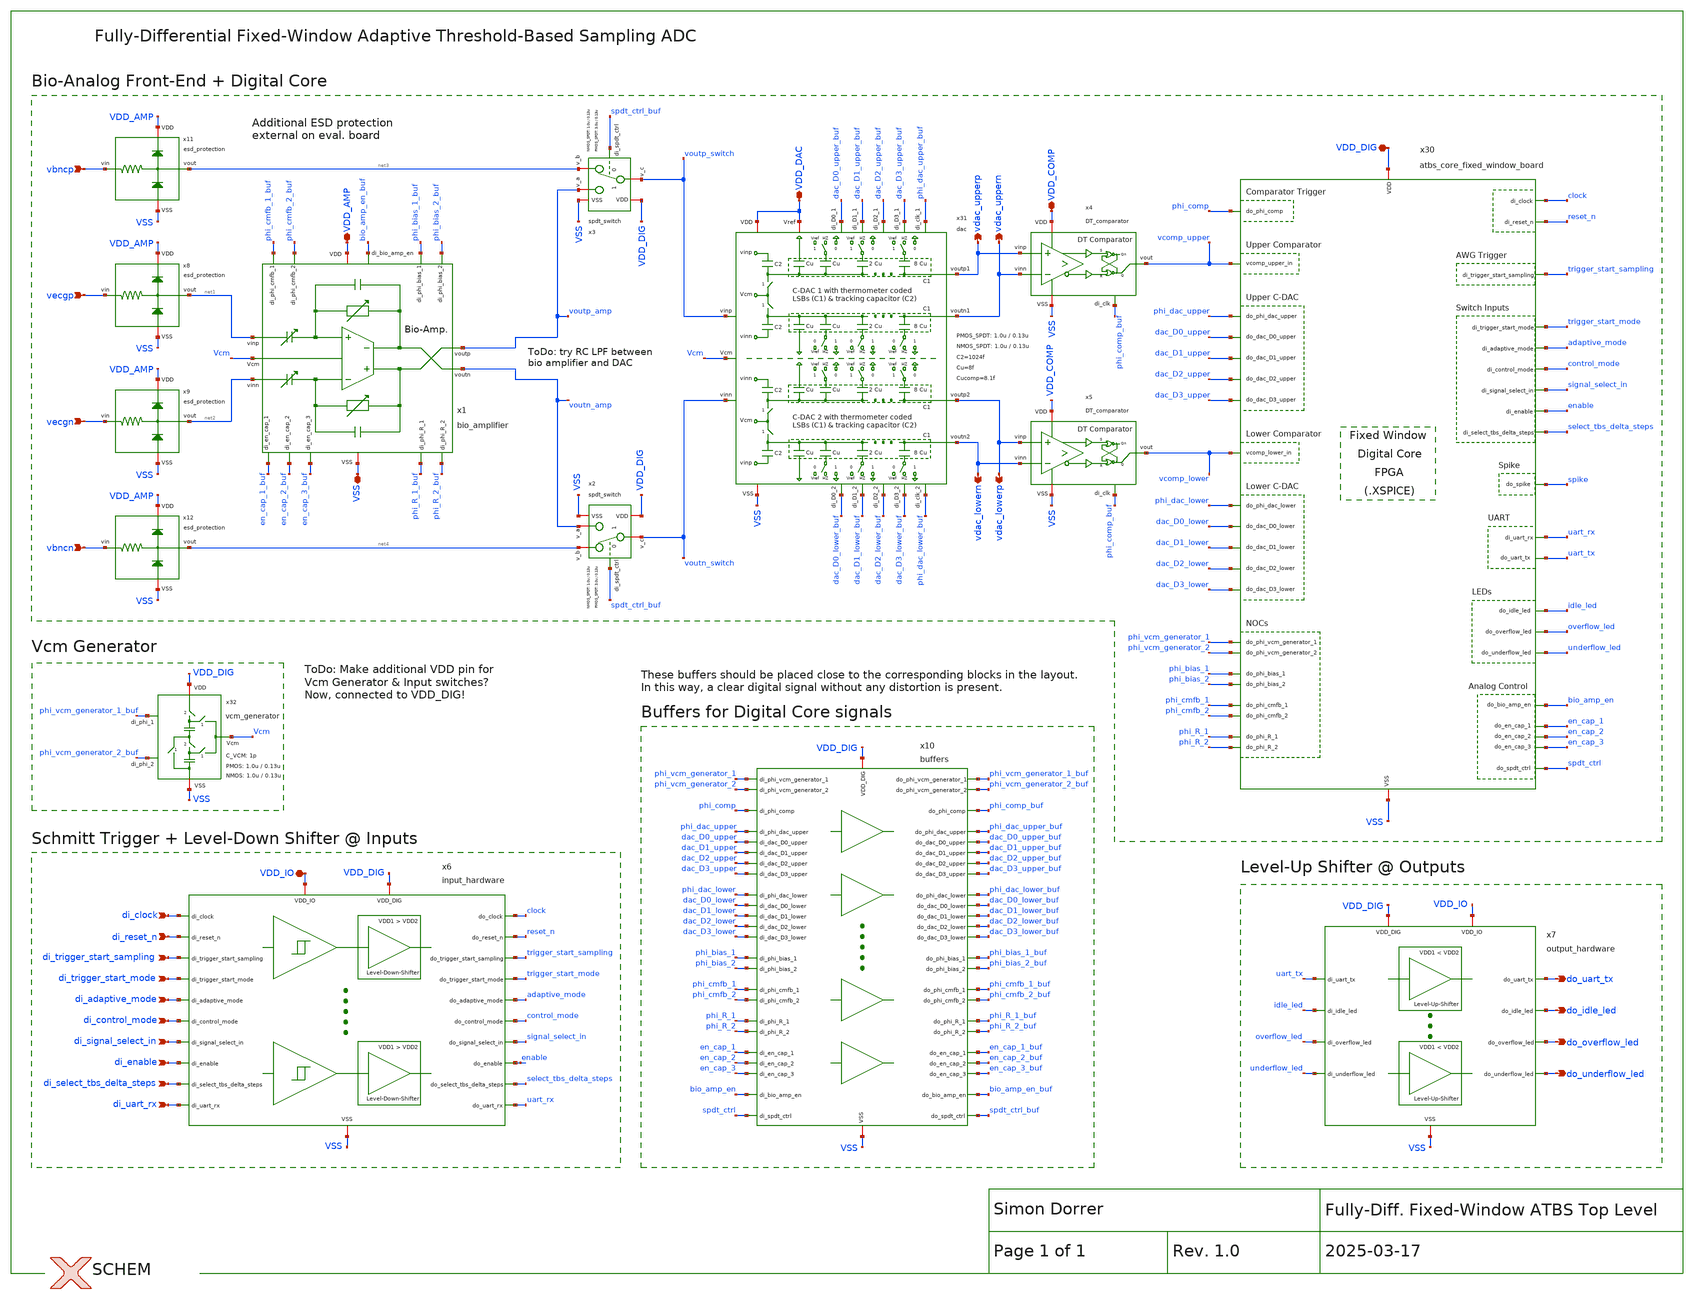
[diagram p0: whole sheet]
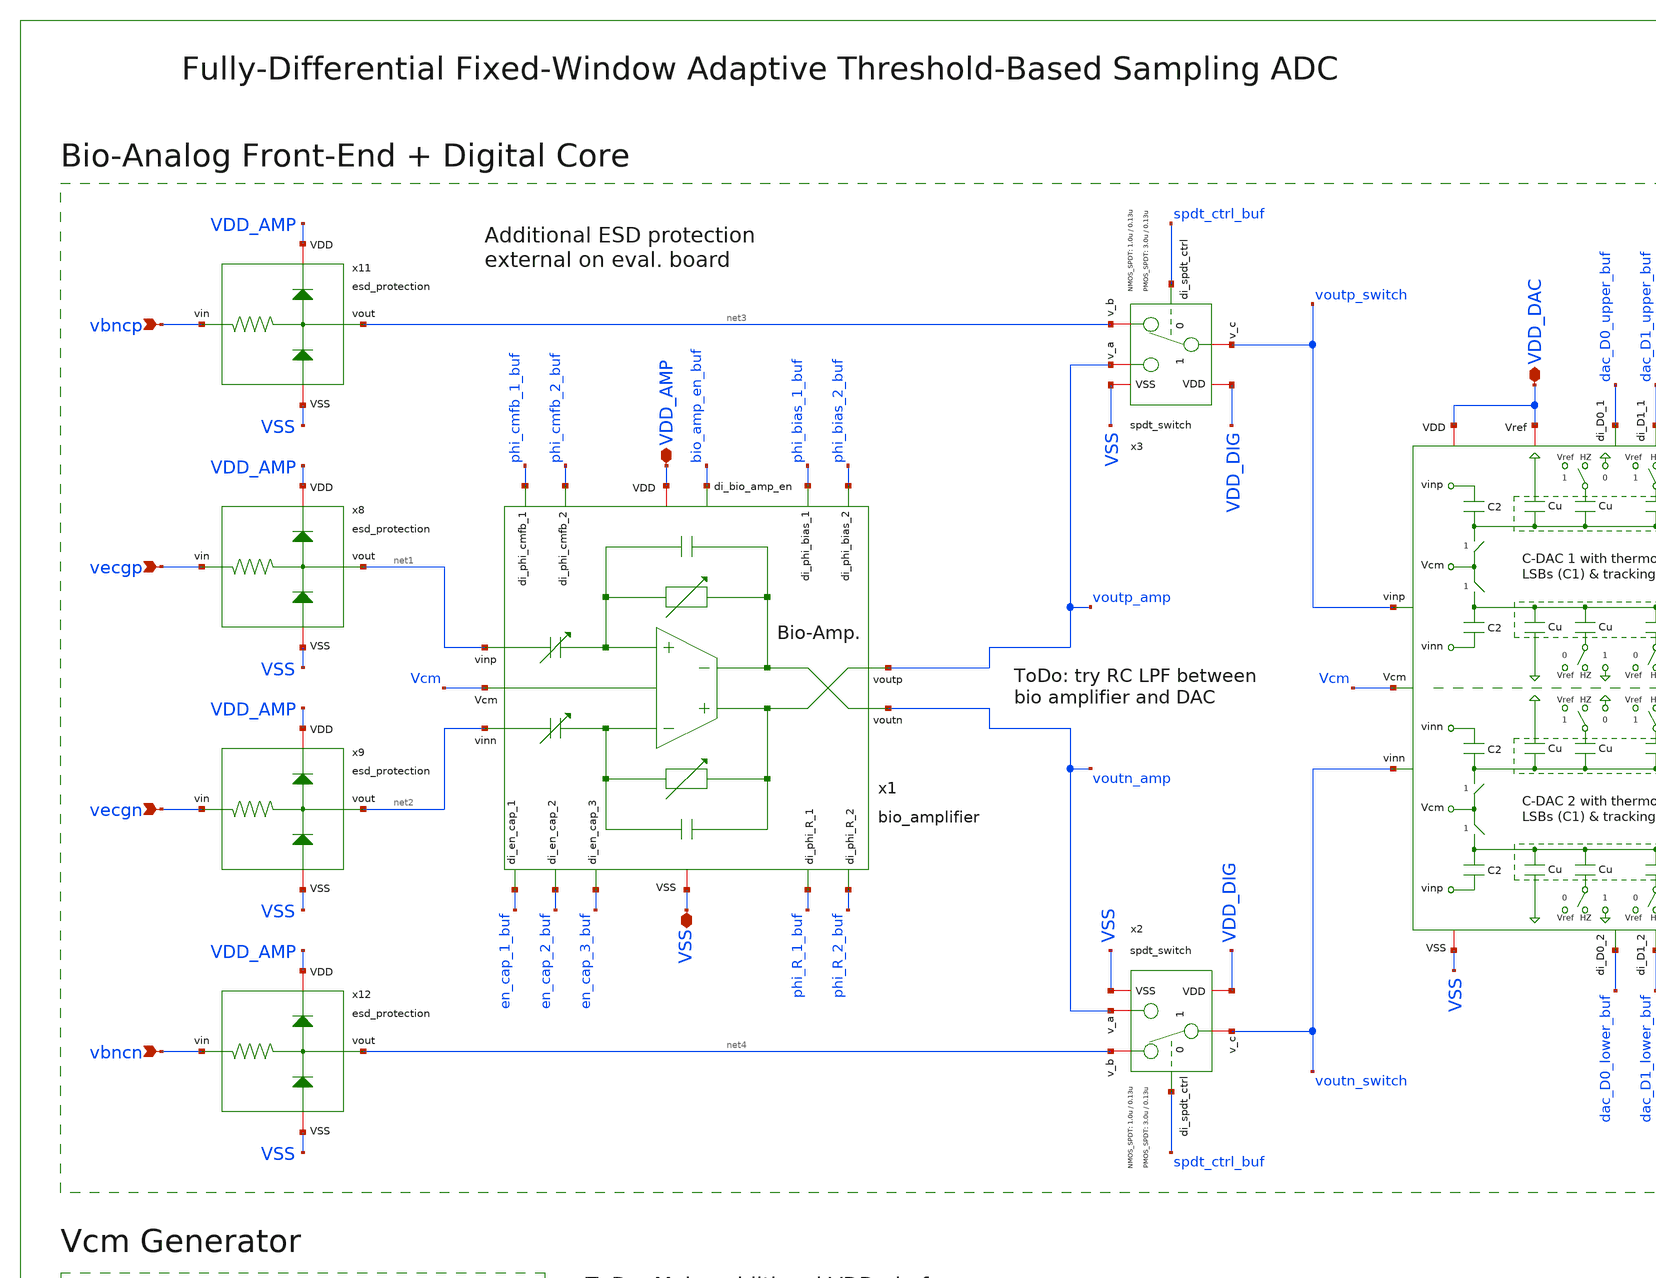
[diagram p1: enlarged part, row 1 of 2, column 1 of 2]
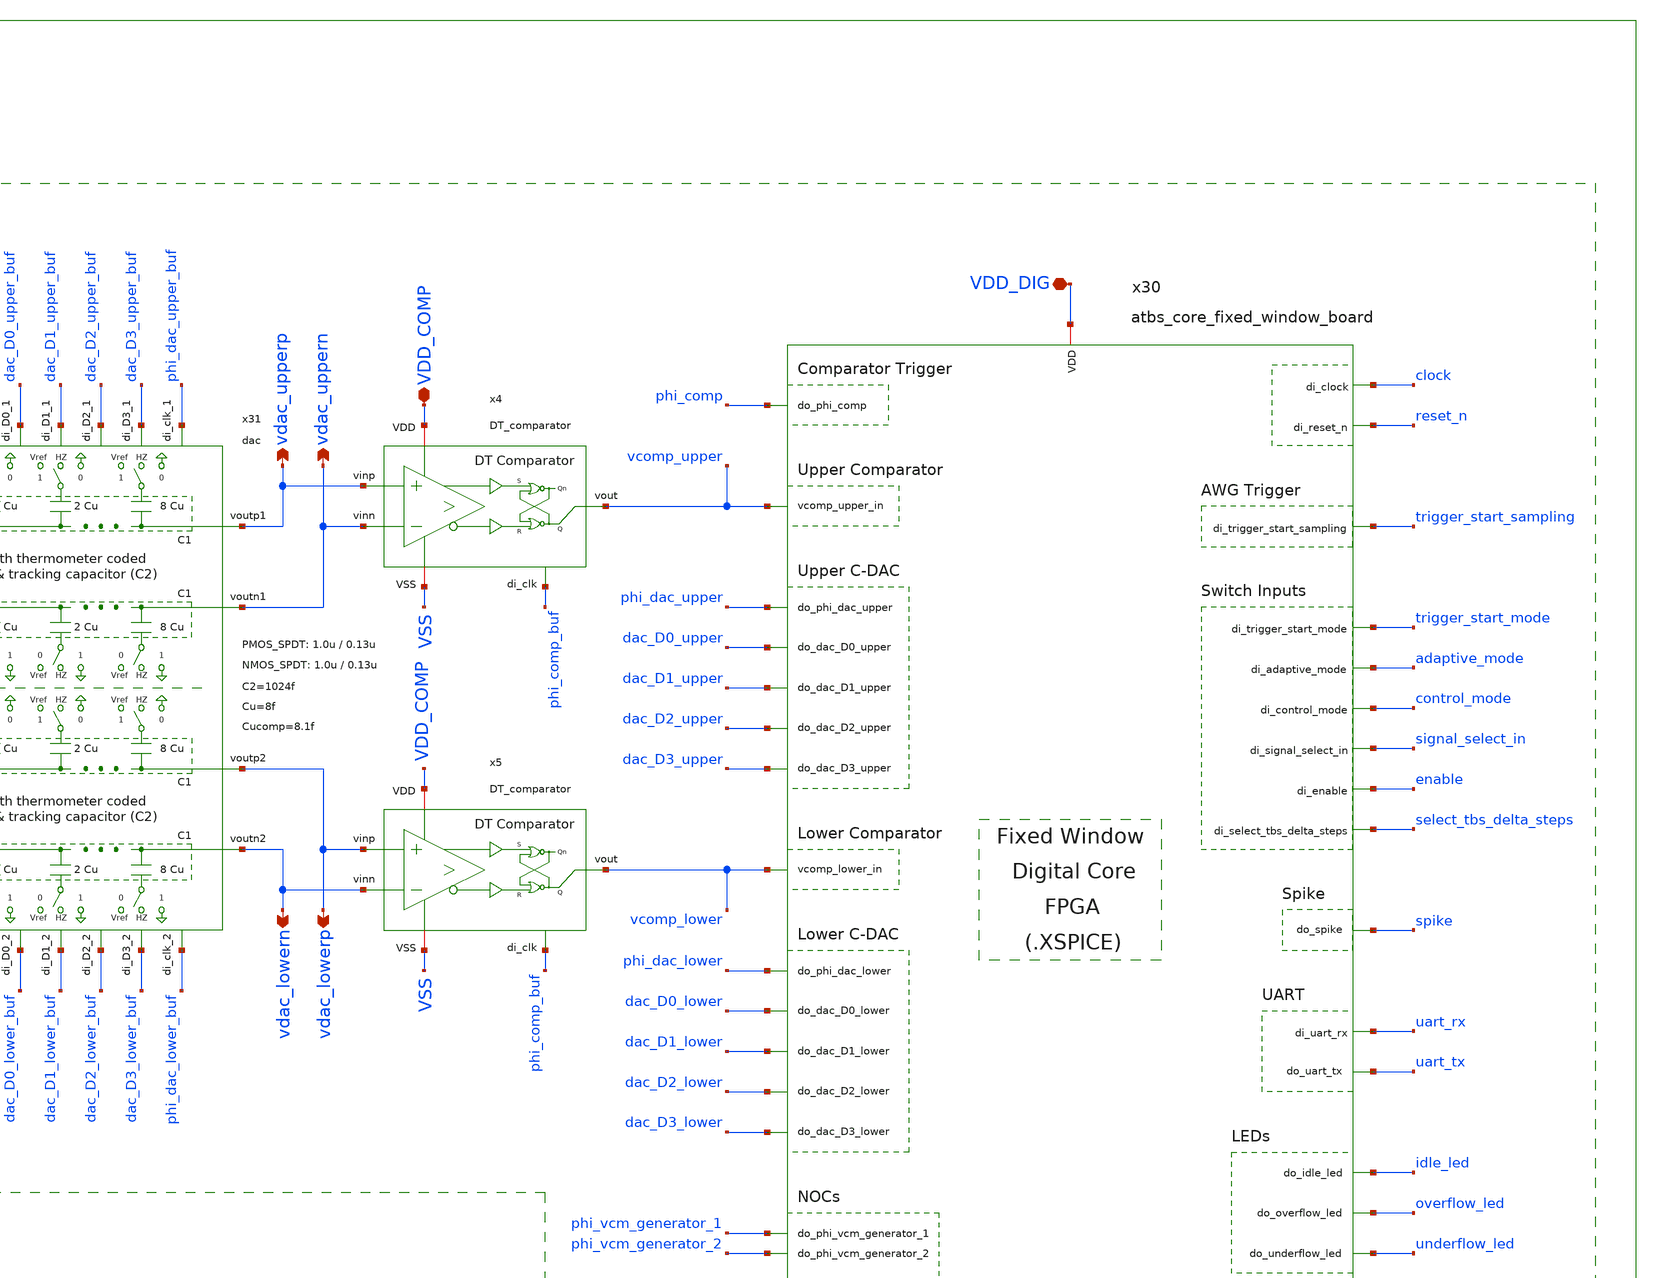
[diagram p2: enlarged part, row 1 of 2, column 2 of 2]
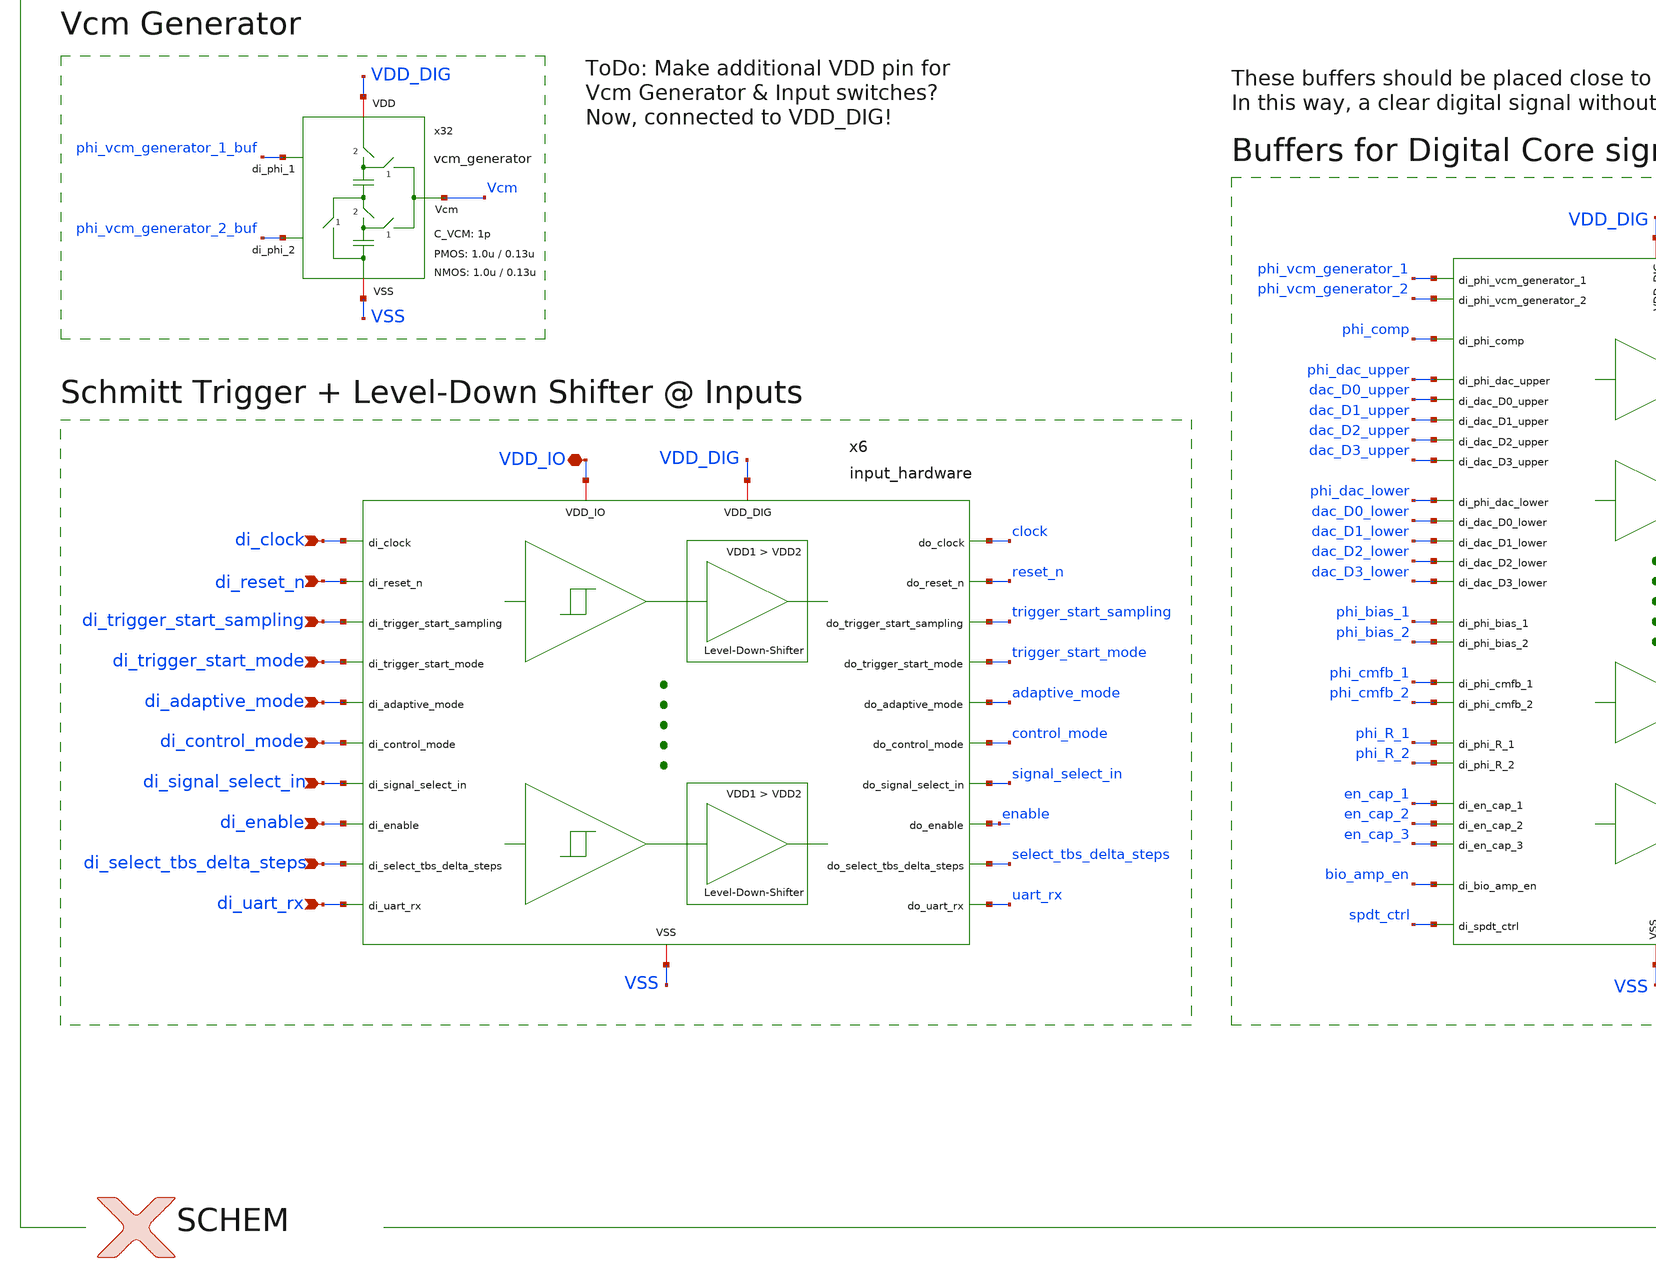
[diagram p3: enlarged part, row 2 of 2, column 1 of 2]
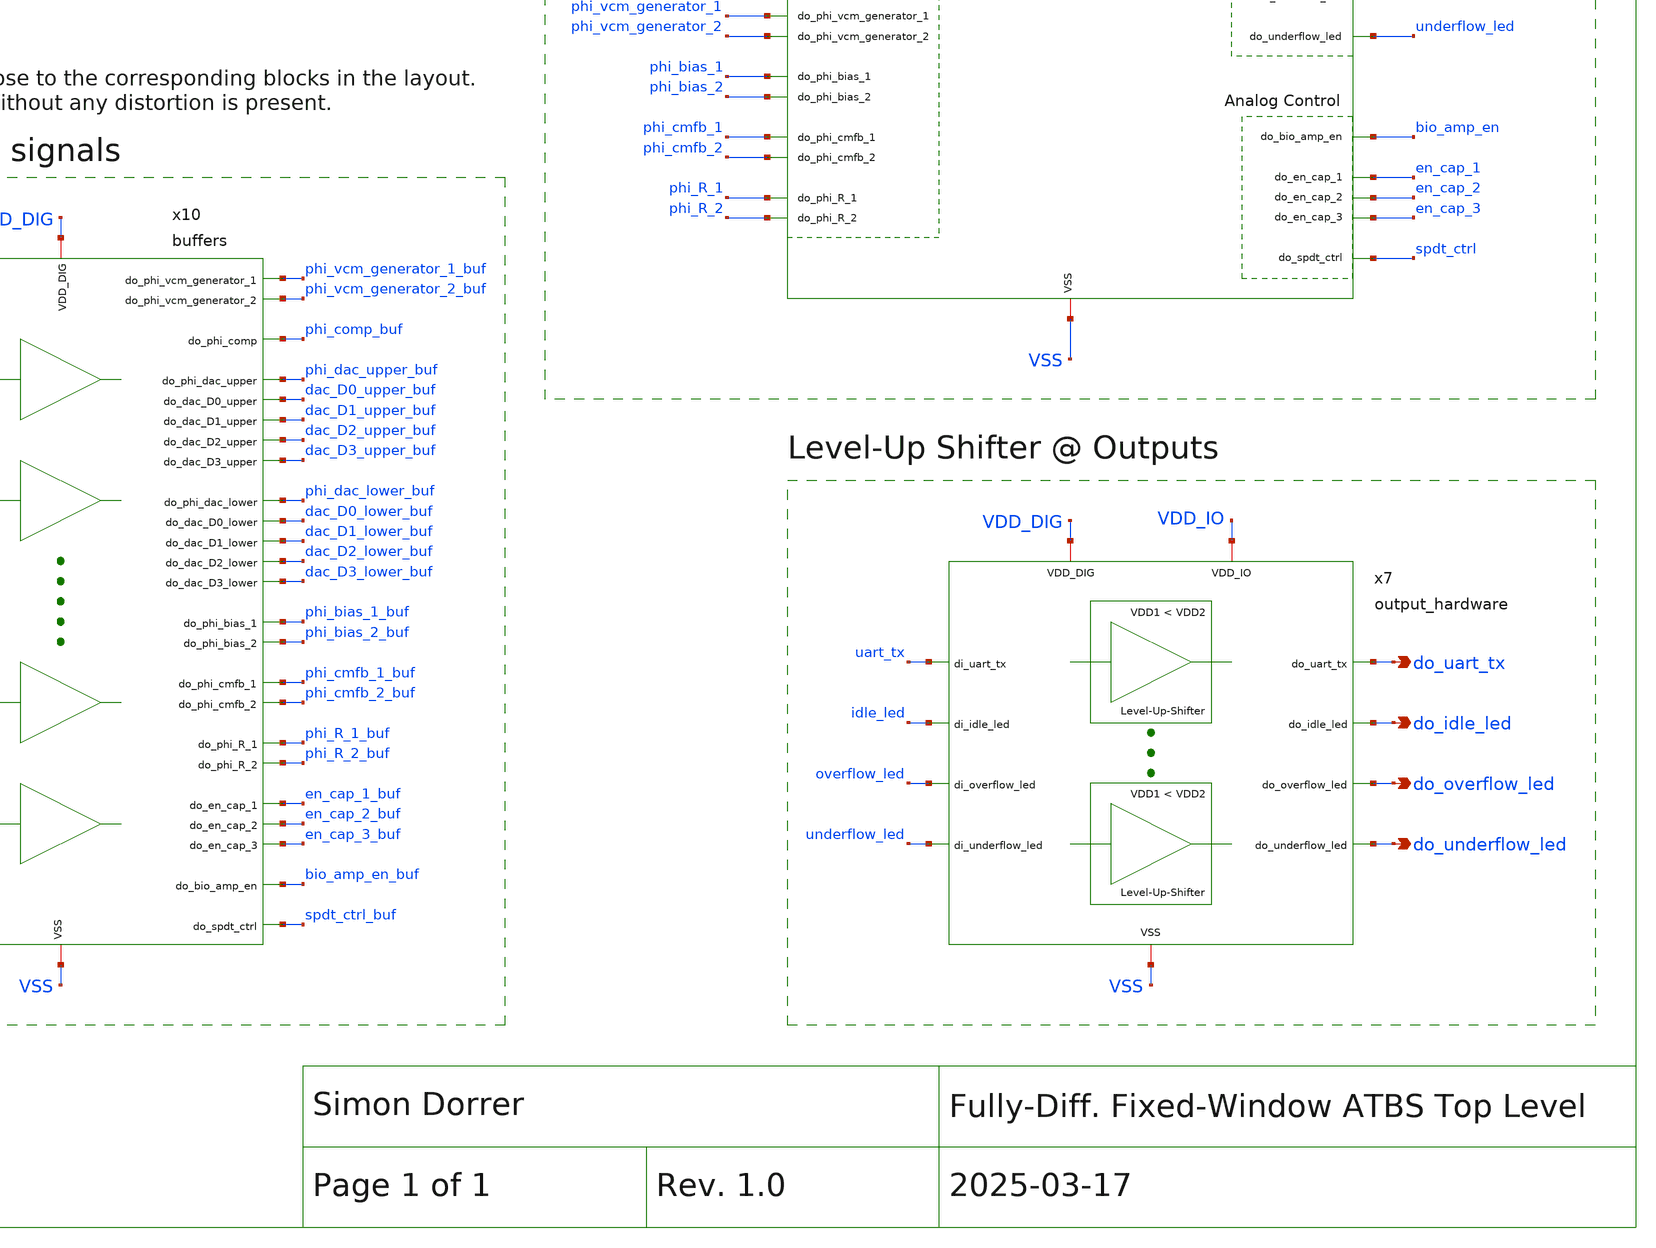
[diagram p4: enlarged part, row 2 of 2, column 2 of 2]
** sch_path: SG13G2_ATBS-ADC-main/xschem/top_level/atbs_top_fixed_window.sch
**.subckt atbs_top_fixed_window VDD_DIG VSS VDD_COMP vecgp di_clock di_reset_n VDD_DAC di_uart_rx
*+ do_uart_tx di_trigger_start_sampling di_trigger_start_mode di_adaptive_mode di_control_mode
*+ di_signal_select_in di_enable di_select_tbs_delta_steps do_idle_led do_overflow_led do_underflow_led vdac_upperp
*+ vdac_lowern VDD_AMP vecgn vbncp vbncn VDD_IO vdac_uppern vdac_lowerp
*.iopin VDD_DIG
*.iopin VSS
*.iopin VDD_COMP
*.ipin vecgp
*.ipin di_clock
*.ipin di_reset_n
*.iopin VDD_DAC
*.ipin di_uart_rx
*.opin do_uart_tx
*.ipin di_trigger_start_sampling
*.ipin di_trigger_start_mode
*.ipin di_adaptive_mode
*.ipin di_control_mode
*.ipin di_signal_select_in
*.ipin di_enable
*.ipin di_select_tbs_delta_steps
*.opin do_idle_led
*.opin do_overflow_led
*.opin do_underflow_led
*.opin vdac_upperp
*.opin vdac_lowern
*.iopin VDD_AMP
*.ipin vecgn
*.ipin vbncp
*.ipin vbncn
*.iopin VDD_IO
*.opin vdac_uppern
*.opin vdac_lowerp
x1 phi_bias_2_buf phi_bias_1_buf phi_R_2_buf phi_R_1_buf en_cap_3_buf en_cap_1_buf en_cap_2_buf
+ phi_cmfb_2_buf phi_cmfb_1_buf voutp_amp bio_amp_en_buf net1 Vcm voutn_amp net2 VDD_AMP VSS bio_amplifier
x2 VDD_DIG spdt_ctrl_buf VSS voutn_switch net4 voutn_amp spdt_switch W_P_TG=3.0u L_P_TG=0.13u
+ W_N_TG=1.0u L_N_TG=0.13u
x3 VDD_DIG spdt_ctrl_buf VSS voutp_switch net3 voutp_amp spdt_switch W_P_TG=3.0u L_P_TG=0.13u
+ W_N_TG=1.0u L_N_TG=0.13u
x4 VDD_COMP vdac_upperp vcomp_upper vdac_uppern phi_comp_buf VSS DT_comparator
x5 VDD_COMP vdac_lowerp vcomp_lower vdac_lowern phi_comp_buf VSS DT_comparator
x30 VDD_DIG VSS adaptive_mode bio_amp_en clock vcomp_lower vcomp_upper control_mode dac_D0_lower
+ dac_D1_lower dac_D2_lower dac_D3_lower dac_D0_upper dac_D1_upper dac_D2_upper dac_D3_upper enable idle_led
+ overflow_led phi_bias_1 phi_bias_2 phi_cmfb_1 phi_cmfb_2 phi_comp phi_dac_lower phi_dac_upper phi_R_1 phi_R_2
+ phi_vcm_generator_1 phi_vcm_generator_2 reset_n en_cap_1 en_cap_2 en_cap_3 spdt_ctrl select_tbs_delta_steps
+ signal_select_in spike trigger_start_mode trigger_start_sampling uart_rx uart_tx underflow_led
+ atbs_core_fixed_window_board
x32 VDD_DIG phi_vcm_generator_2_buf phi_vcm_generator_1_buf Vcm VSS vcm_generator C_VCM=1p
+ W_P_VCM=1.0u L_P_VCM=0.13u W_N_VCM=1.0u L_N_VCM=0.13u
x31 VDD_DAC voutp_switch vdac_upperp vdac_uppern voutn_switch dac_D0_lower_buf dac_D1_lower_buf
+ dac_D2_lower_buf dac_D3_lower_buf VSS VDD_DAC Vcm vdac_lowerp vdac_lowern phi_dac_lower_buf dac_D0_upper_buf
+ dac_D1_upper_buf dac_D2_upper_buf dac_D3_upper_buf phi_dac_upper_buf dac W_P_SPDT=1.0u L_P_SPDT=0.13u W_N_SPDT=1.0u
+ L_N_SPDT=0.13u C2=1024f Cu=8f Cucomp=8.1f
x6 VDD_IO di_clock di_control_mode clock control_mode VSS di_reset_n reset_n di_signal_select_in
+ signal_select_in enable trigger_start_sampling di_trigger_start_sampling di_enable select_tbs_delta_steps
+ di_select_tbs_delta_steps trigger_start_mode di_trigger_start_mode di_adaptive_mode uart_rx adaptive_mode di_uart_rx VDD_DIG
+ input_hardware
x7 uart_tx do_uart_tx do_idle_led idle_led do_overflow_led overflow_led underflow_led
+ do_underflow_led VDD_IO VSS VDD_DIG output_hardware
x8 VDD_AMP vecgp net1 VSS esd_protection
x9 VDD_AMP vecgn net2 VSS esd_protection
x10 VDD_DIG phi_dac_lower phi_bias_1_buf phi_dac_upper phi_cmfb_1 phi_dac_lower_buf phi_cmfb_1_buf
+ phi_bias_1 phi_dac_upper_buf VSS dac_D0_lower dac_D0_lower_buf phi_cmfb_2 phi_bias_2_buf phi_bias_2
+ dac_D0_upper dac_D0_upper_buf phi_cmfb_2_buf dac_D1_upper phi_R_1_buf phi_R_1 en_cap_1_buf dac_D1_lower_buf
+ dac_D1_upper_buf dac_D1_lower en_cap_1 dac_D2_upper phi_R_2_buf phi_R_2 en_cap_2_buf dac_D2_lower_buf en_cap_2
+ dac_D2_lower dac_D2_upper_buf bio_amp_en_buf en_cap_3_buf en_cap_3 bio_amp_en dac_D3_upper_buf dac_D3_lower_buf
+ dac_D3_lower dac_D3_upper phi_comp phi_vcm_generator_1_buf phi_vcm_generator_1 spdt_ctrl_buf spdt_ctrl
+ phi_comp_buf phi_vcm_generator_2_buf phi_vcm_generator_2 buffers
x11 VDD_AMP vbncp net3 VSS esd_protection
x12 VDD_AMP vbncn net4 VSS esd_protection
**.ends
.end
